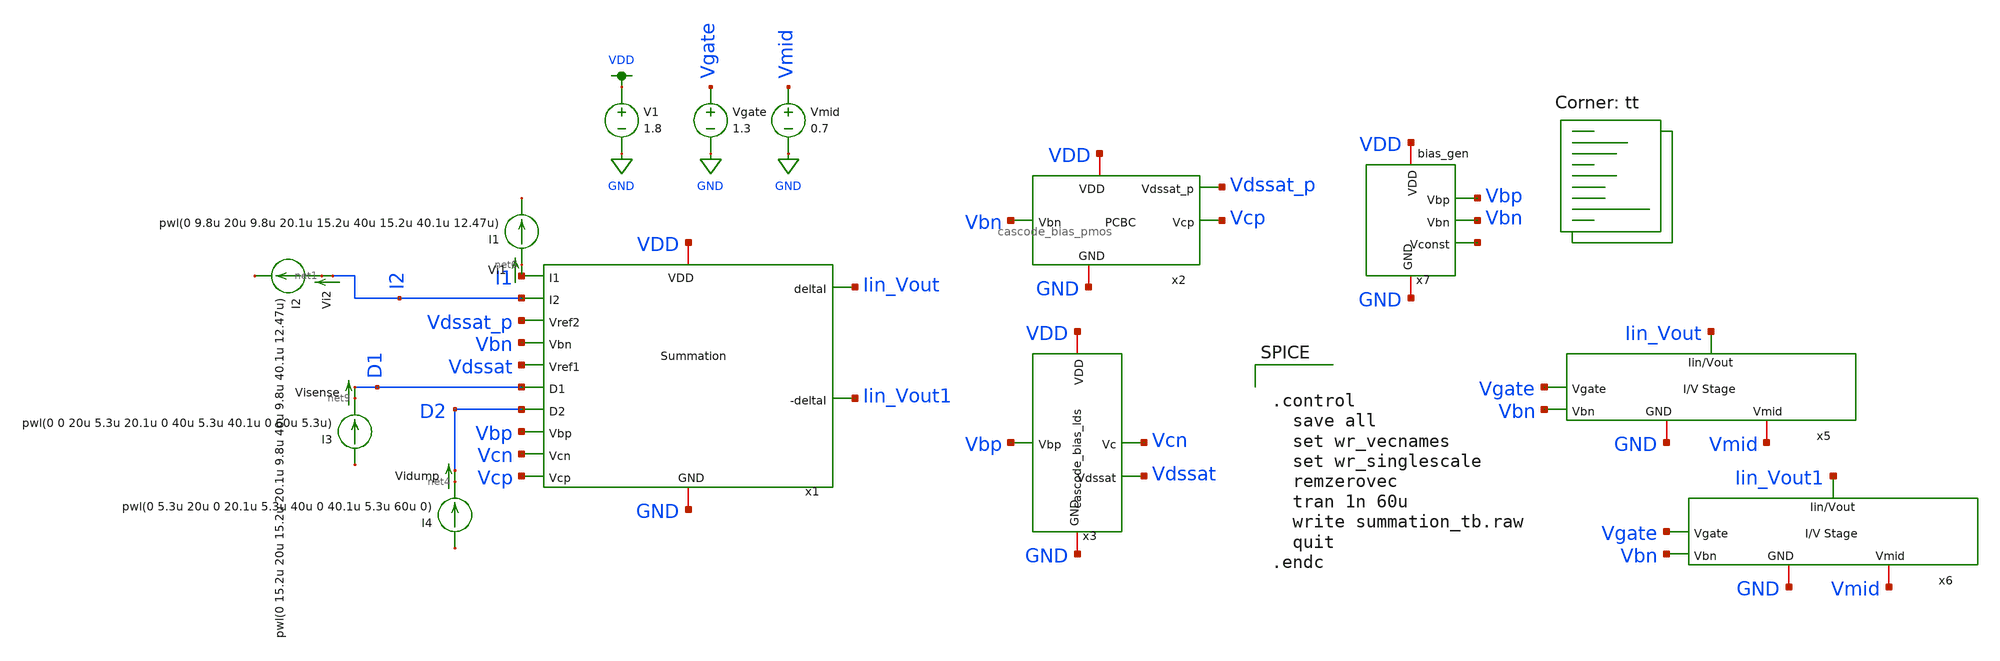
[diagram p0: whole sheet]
** sch_path: final/schematics/summation_tb.sch
**.subckt summation_tb
x1 VDD GND I1 I2 Vdssat_p Vbn Vdssat D1 D2 Iin_Vout Iin_Vout1 Vbp Vcn Vcp summation
x2 Vbn VDD GND Vcp Vdssat_p cascode_bias_pmos
x3 Vbp VDD Vcn GND Vdssat cascode_bias_lds
I2 net1 net2 pwl(0 15.2u 20u 15.2u 20.1u 9.8u 40u 9.8u 40.1u 12.47u)
I4 net3 net4 pwl(0 5.3u 20u 0 20.1u 5.3u 40u 0 40.1u 5.3u 60u 0)
V1 VDD GND 1.8
x5 Iin_Vout Vgate Vmid Vbn GND IV_converter
x6 Iin_Vout1 Vgate Vmid Vbn GND IV_converter
Vgate Vgate GND 1.3
Vmid Vmid GND 0.7
x7 VDD Vbp net5 GND Vbn bias_gen
I1 net6 net7 pwl(0 9.8u 20u 9.8u 20.1u 15.2u 40u 15.2u 40.1u 12.47u)
I3 net8 net9 pwl(0 0 20u 5.3u 20.1u 0 40u 5.3u 40.1u 0 60u 5.3u)
Vidump net4 D2 0
.save i(vidump)
Visense net9 D1 0
.save i(visense)
Vi2 I2 net1 0
.save i(vi2)
Vi1 I1 net6 0
.save i(vi1)
**** begin user architecture code


.control
  save all
  set wr_vecnames
  set wr_singlescale
  remzerovec
  tran 1n 60u
  write summation_tb.raw
  quit
.endc


.lib $::SKYWATER_MODELS/sky130.lib.spice tt
**** end user architecture code
**.ends
.GLOBAL VDD
.GLOBAL GND
.end
